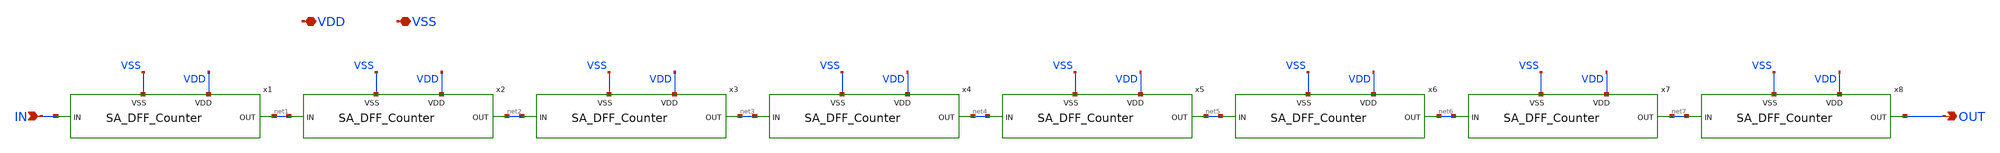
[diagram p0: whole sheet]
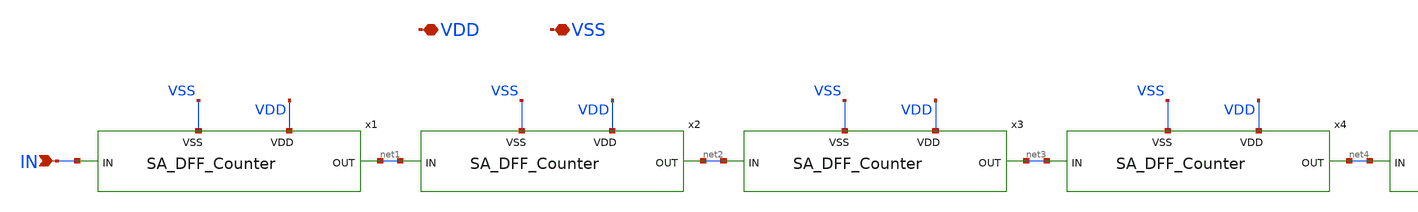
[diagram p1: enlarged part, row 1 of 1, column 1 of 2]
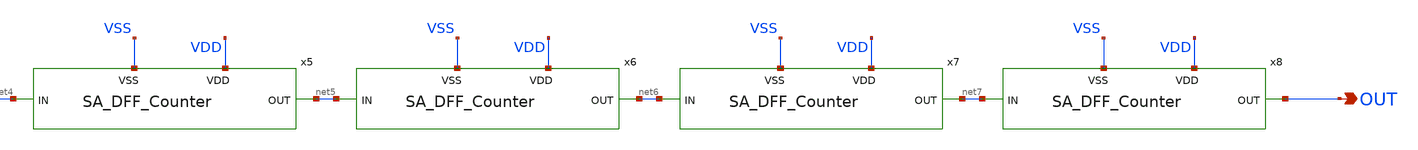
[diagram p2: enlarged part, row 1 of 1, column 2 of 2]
** sch_path: design/xschem/VCO/SA_DFF_Counter_8.sch
**.subckt SA_DFF_Counter_8 IN VDD VSS OUT
*.ipin IN
*.iopin VDD
*.iopin VSS
*.opin OUT
x1 VDD VSS net1 IN SA_DFF_Counter
x2 VDD VSS net2 net1 SA_DFF_Counter
x3 VDD VSS net3 net2 SA_DFF_Counter
x4 VDD VSS net4 net3 SA_DFF_Counter
x5 VDD VSS net5 net4 SA_DFF_Counter
x6 VDD VSS net6 net5 SA_DFF_Counter
x7 VDD VSS net7 net6 SA_DFF_Counter
x8 VDD VSS OUT net7 SA_DFF_Counter
**.ends

* expanding   symbol:  VCO/SA_DFF_Counter.sym # of pins=4
** sym_path: design/xschem/VCO/SA_DFF_Counter.sym
** sch_path: design/xschem/VCO/SA_DFF_Counter.sch
.subckt SA_DFF_Counter VDD VSS OUT IN
*.ipin IN
*.iopin VDD
*.iopin VSS
*.opin OUT
x2 IN IN net1 VDD VSS OUT net1 dff1
.ends

.end
